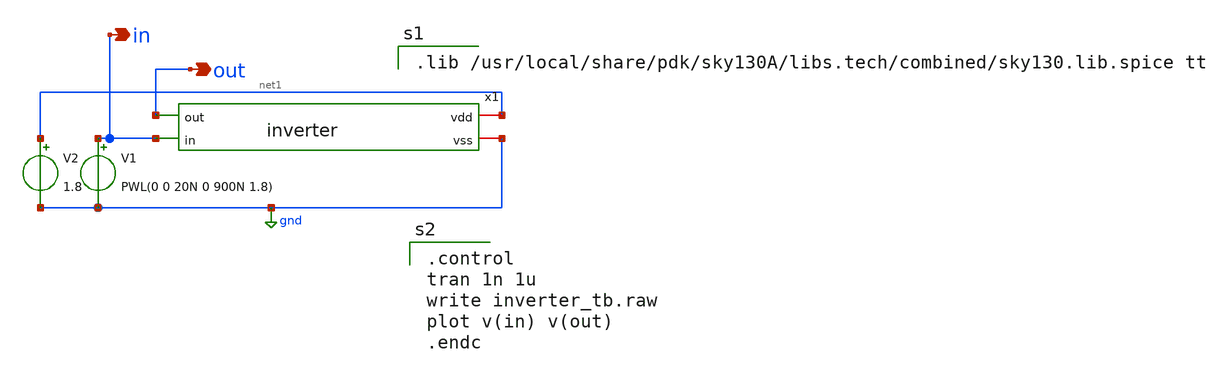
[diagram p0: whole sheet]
** sch_path: xschem/inverter_tb.sch
**.subckt inverter_tb out in
*.opin out
*.opin in
x1 net1 out in gnd inverter
V1 in gnd PWL(0 0 20N 0 900N 1.8)
V2 net1 gnd 1.8
**** begin user architecture code

.lib /usr/local/share/pdk/sky130A/libs.tech/combined/sky130.lib.spice tt


.control
tran 1n 1u
write inverter_tb.raw
plot v(in) v(out)
.endc

**** end user architecture code
**.ends

* expanding   symbol:  inverter.sym # of pins=4
** sym_path: xschem/inverter.sym
** sch_path: xschem/inverter.sch
.subckt inverter vdd out in vss
*.iopin vdd
*.ipin in
*.ipin out
*.iopin vss
XM1 out in vss vss sky130_fd_pr__nfet_01v8 L=0.18 W=4.5 nf=3 ad='int((3 + 1)/2) * 4.5 / 3 * 0.29' as='int((3 + 2)/2) * 4.5 / 3 * 0.29'
+ pd='2*int((3 + 1)/2) * (4.5 / 3 + 0.29)' ps='2*int((3 + 2)/2) * (4.5 / 3 + 0.29)' nrd='0.29 / 4.5 ' nrs='0.29 / 4.5 '
+ sa=0 sb=0 sd=0 mult=1 m=1
XM2 out in vdd VDD sky130_fd_pr__pfet_01v8 L=0.18 W=3 nf=3 ad='int((3 + 1)/2) * 3 / 3 * 0.29' as='int((3 + 2)/2) * 3 / 3 * 0.29'
+ pd='2*int((3 + 1)/2) * (3 / 3 + 0.29)' ps='2*int((3 + 2)/2) * (3 / 3 + 0.29)' nrd='0.29 / 3 ' nrs='0.29 / 3 '
+ sa=0 sb=0 sd=0 mult=1 m=1
.ends

.GLOBAL gnd
.end
